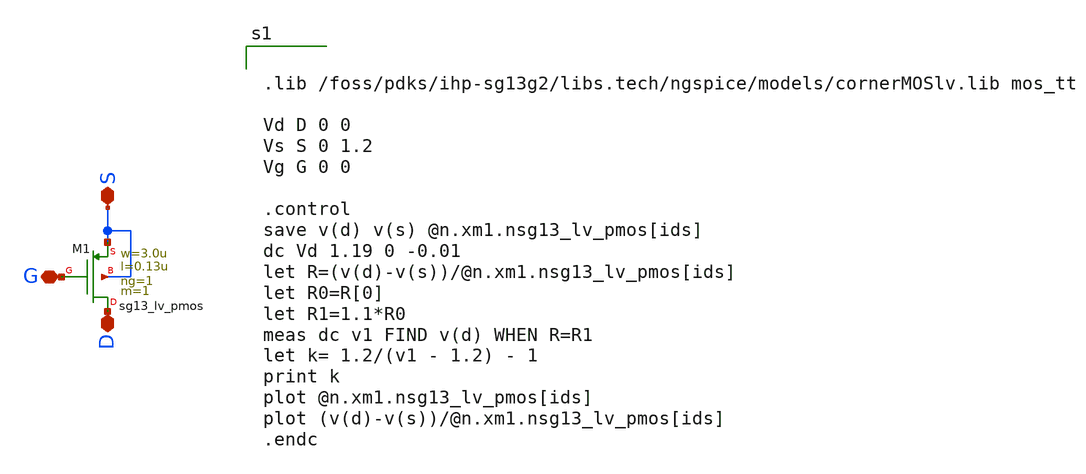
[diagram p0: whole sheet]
** sch_path: xschem/pmos_tb.sch
**.subckt pmos_tb S G D
*.iopin S
*.iopin G
*.iopin D
XM1 D G S S sg13_lv_pmos w=3.0u l=0.13u ng=1 m=1 mm_ok=1
**** begin user architecture code


.lib /foss/pdks/ihp-sg13g2/libs.tech/ngspice/models/cornerMOSlv.lib mos_tt

Vd D 0 0
Vs S 0 1.2
Vg G 0 0

.control
save v(d) v(s) @n.xm1.nsg13_lv_pmos[ids]
dc Vd 1.19 0 -0.01
let R=(v(d)-v(s))/@n.xm1.nsg13_lv_pmos[ids]
let R0=R[0]
let R1=1.1*R0
meas dc v1 FIND v(d) WHEN R=R1
let k= 1.2/(v1 - 1.2) - 1
print k
plot @n.xm1.nsg13_lv_pmos[ids]
plot (v(d)-v(s))/@n.xm1.nsg13_lv_pmos[ids]
.endc


**** end user architecture code
**.ends
.end
